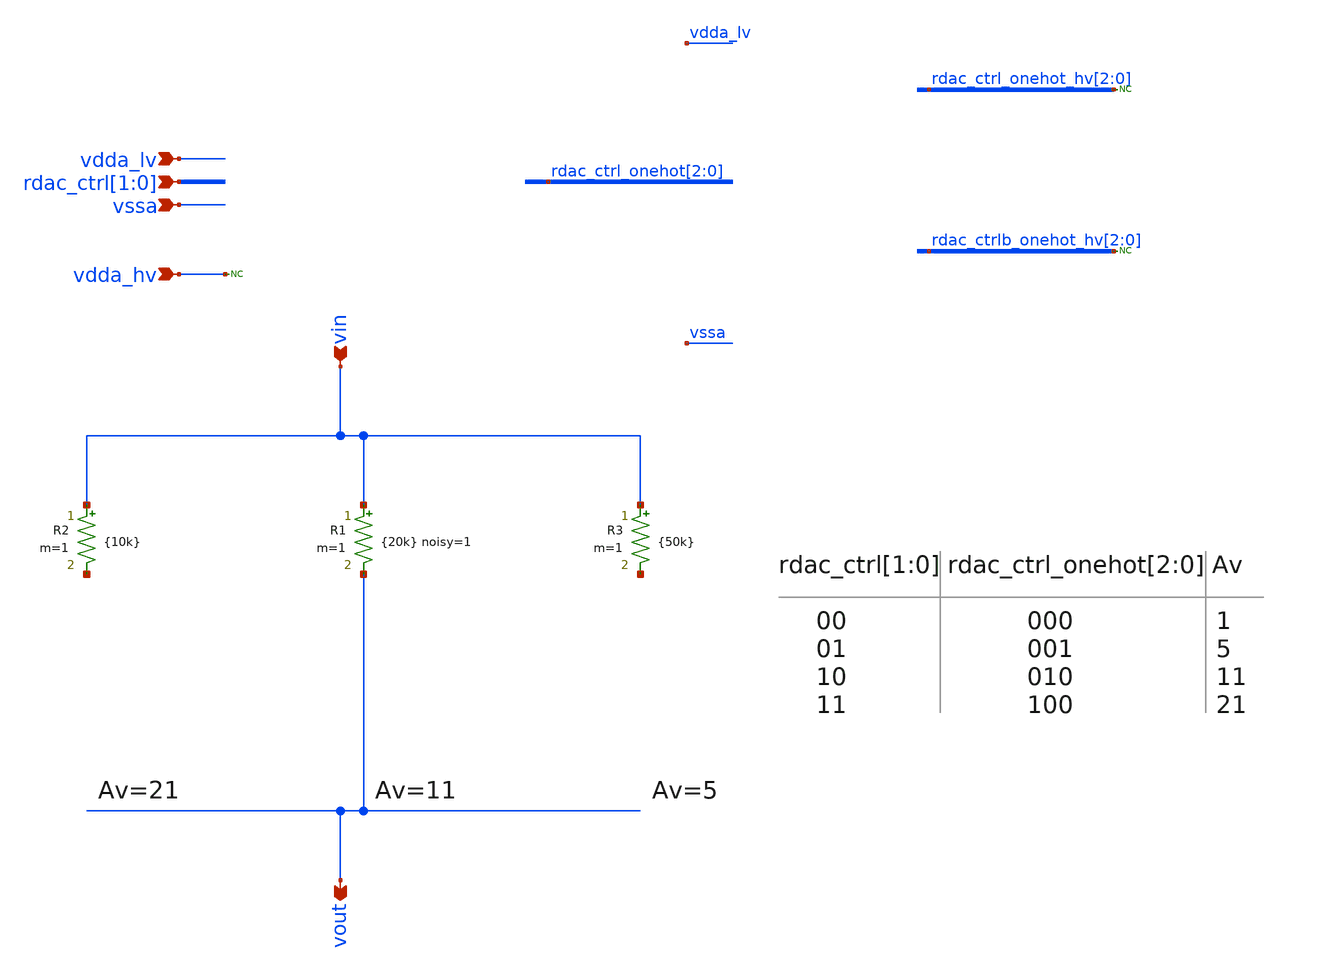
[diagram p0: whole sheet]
** sch_path: Design_Review_1/Testbench_3_tb_sunrise_ina_CMR_idealR/rdac_no_sws_av11.sch
**.subckt rdac_no_sws_av11 vin vout vdda_lv vssa rdac_ctrl[1],rdac_ctrl[0] vdda_hv
*.ipin vin
*.opin vout
*.ipin vdda_lv
*.ipin vssa
*.ipin rdac_ctrl[1],rdac_ctrl[0]
*.ipin vdda_hv
R2 vin net1 {10k} m=1
R1 vin vout {20k} noisy=1 m=1
R3 vin net2 {50k} m=1
* noconn vdda_hv
* noconn rdac_ctrl_onehot_hv[2:0]
* noconn rdac_ctrlb_onehot_hv[2:0]
**.ends
.end
